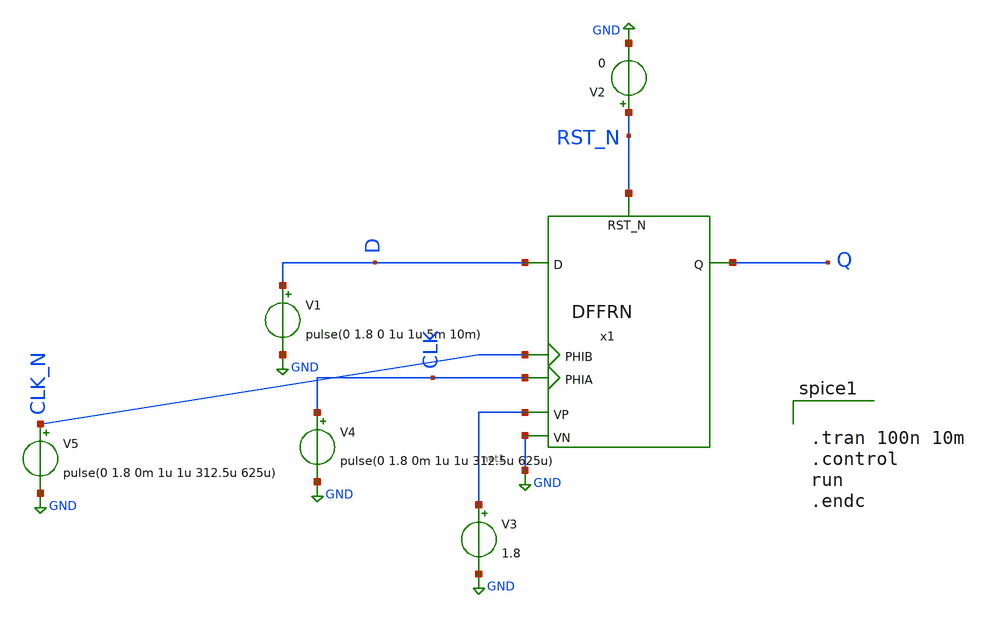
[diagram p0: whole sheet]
** sch_path: ADC/16bit_C2C/MagicAndSpice/EE431_FinalProj/DFFR_tb.sch
**.subckt DFFR_tb
V2 RST_N GND 0
x1 CLK CLK_N D Q RST_N net1 GND DFFRN
V3 net1 GND 1.8
V4 CLK GND pulse(0 1.8 0m 1u 1u 312.5u 625u)
V1 D GND pulse(0 1.8 0 1u 1u 5m 10m)
V5 CLK_N GND pulse(0 1.8 0m 1u 1u 312.5u 625u)
**** begin user architecture code
 .lib $::SKYWATER_MODELS/sky130.lib.spice tt


.tran 100n 10m
.control
run
.endc

**** end user architecture code
**.ends
.GLOBAL GND
.end
